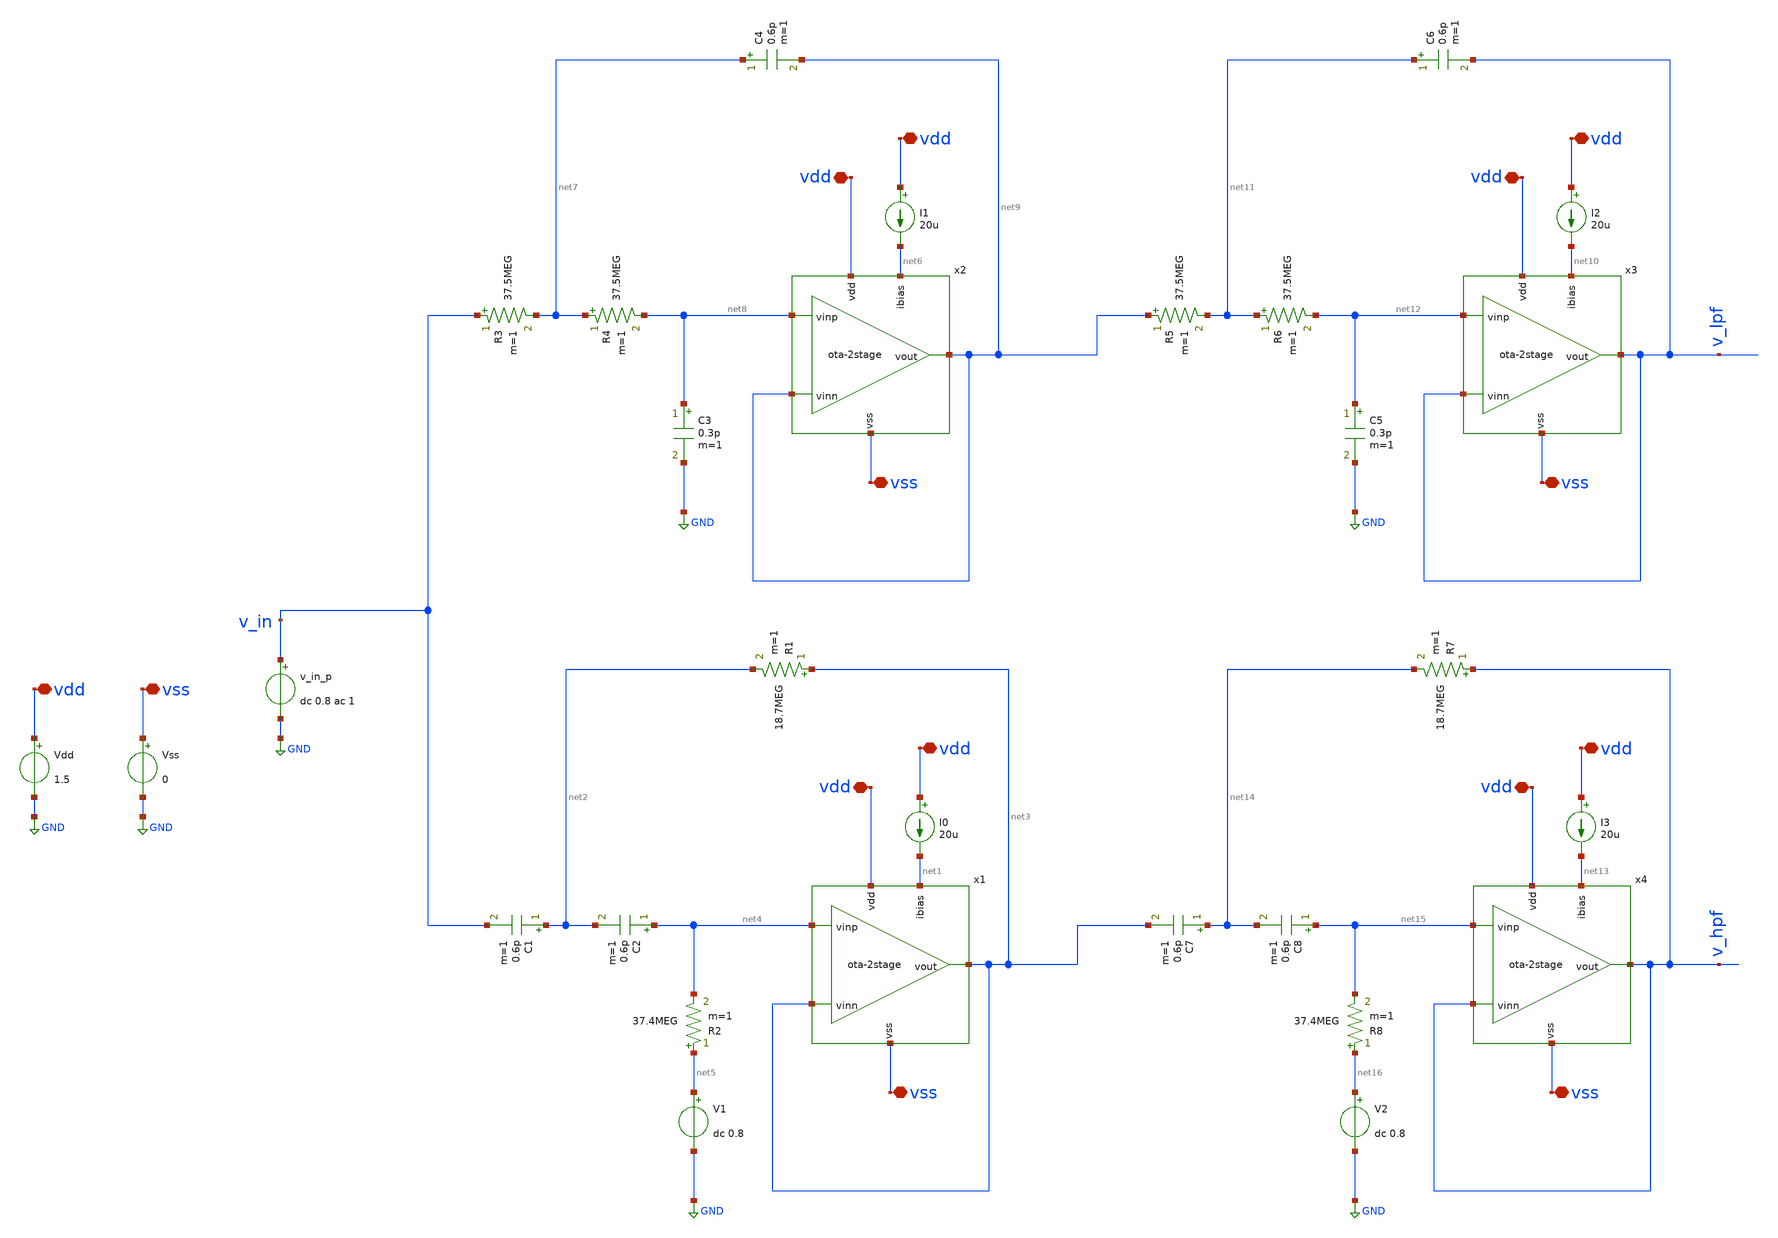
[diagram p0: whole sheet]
** sch_path: testbench/ota-2stage_tb-sk-LR4.sch
**.subckt ota-2stage_tb-sk-LR4 vdd vdd vdd vss vss vdd vdd vss vdd vdd vss vdd vdd vss
*.iopin vdd
*.iopin vdd
*.iopin vdd
*.iopin vss
*.iopin vss
*.iopin vdd
*.iopin vdd
*.iopin vss
*.iopin vdd
*.iopin vdd
*.iopin vss
*.iopin vdd
*.iopin vdd
*.iopin vss
I0 vdd net1 20u
Vdd vdd GND 1.5
Vss vss GND 0
v_in_p v_in GND dc 0.8 ac 1
x1 vdd net1 net3 net3 net4 vss ota-2stage
R1 net3 net2 18.7MEG m=1
R2 net5 net4 37.4MEG m=1
C1 net2 v_in 0.6p m=1
C2 net4 net2 0.6p m=1
V1 net5 GND dc 0.8
I1 vdd net6 20u
R3 v_in net7 37.5MEG m=1
R4 net7 net8 37.5MEG m=1
C3 net8 GND 0.3p m=1
C4 net7 net9 0.6p m=1
x2 vdd net6 net9 net9 net8 vss ota-2stage
I2 vdd net10 20u
R5 net9 net11 37.5MEG m=1
R6 net11 net12 37.5MEG m=1
C5 net12 GND 0.3p m=1
C6 net11 v_lpf 0.6p m=1
x3 vdd net10 v_lpf v_lpf net12 vss ota-2stage
I3 vdd net13 20u
x4 vdd net13 v_hpf v_hpf net15 vss ota-2stage
R7 v_hpf net14 18.7MEG m=1
R8 net16 net15 37.4MEG m=1
C7 net14 net3 0.6p m=1
C8 net15 net14 0.6p m=1
V2 net16 GND dc 0.8
**** begin user architecture code


.temp 27
.control
option sparse
save all

* Sweep from 100 Hz to 1 MHz
ac dec 101 100 10MEG

* Plot the response to see your beautiful 10kHz cutoff!
let LPF = 20*log10(v(v_lpf))
let HPF = 20*log10(v(v_hpf))
let SUM = 20*log10(v(v_lpf) + v(v_hpf))
let DIF = 20*log10(v(v_lpf) - v(v_hpf))
plot LPF HPF SUM DIF

* Calculate the exact -3dB cutoff frequency
meas ac dcgain MAX vmag(v_out) FROM=50k TO=0.5MEG
let f3db_target = dcgain / sqrt(2)
meas ac fbw WHEN vmag(v_out)=f3db_target RISE=1

print dcgain
print fbw
.endc


 .lib cornerMOSlv.lib mos_tt
.lib cornerCAP.lib cap_typ
.lib cornerRES.lib res_typ

**** end user architecture code
**.ends
.GLOBAL GND
.end
